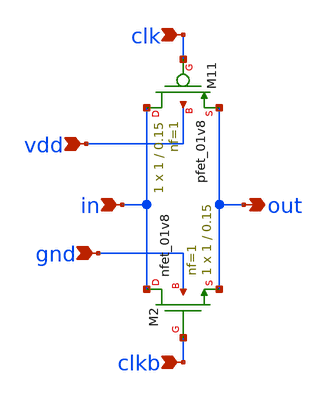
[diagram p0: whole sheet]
** sch_path: pll/dividers_lib/divider_init/xschem/TG.sch
**.subckt TG vdd in gnd clkb clk out
*.ipin vdd
*.ipin in
*.ipin gnd
*.ipin clkb
*.ipin clk
*.opin out
XM11 in clk out vdd sky130_fd_pr__pfet_01v8 L=0.15 W=1 nf=1 ad='int((nf+1)/2) * W/nf * 0.29' as='int((nf+2)/2) * W/nf * 0.29'
+ pd='2*int((nf+1)/2) * (W/nf + 0.29)' ps='2*int((nf+2)/2) * (W/nf + 0.29)' nrd='0.29 / W' nrs='0.29 / W'
+ sa=0 sb=0 sd=0 mult=1 m=1
XM2 in clkb out gnd sky130_fd_pr__nfet_01v8 L=0.15 W=1 nf=1 ad='int((1 + 1)/2) * 1 / 1 * 0.29' as='int((1 + 2)/2) * 1 / 1 * 0.29'
+ pd='2*int((1 + 1)/2) * (1 / 1 + 0.29)' ps='2*int((1 + 2)/2) * (1 / 1 + 0.29)' nrd='0.29 / 1 ' nrs='0.29 / 1 '
+ sa=0 sb=0 sd=0 mult=1 m=1
**.ends
.end
